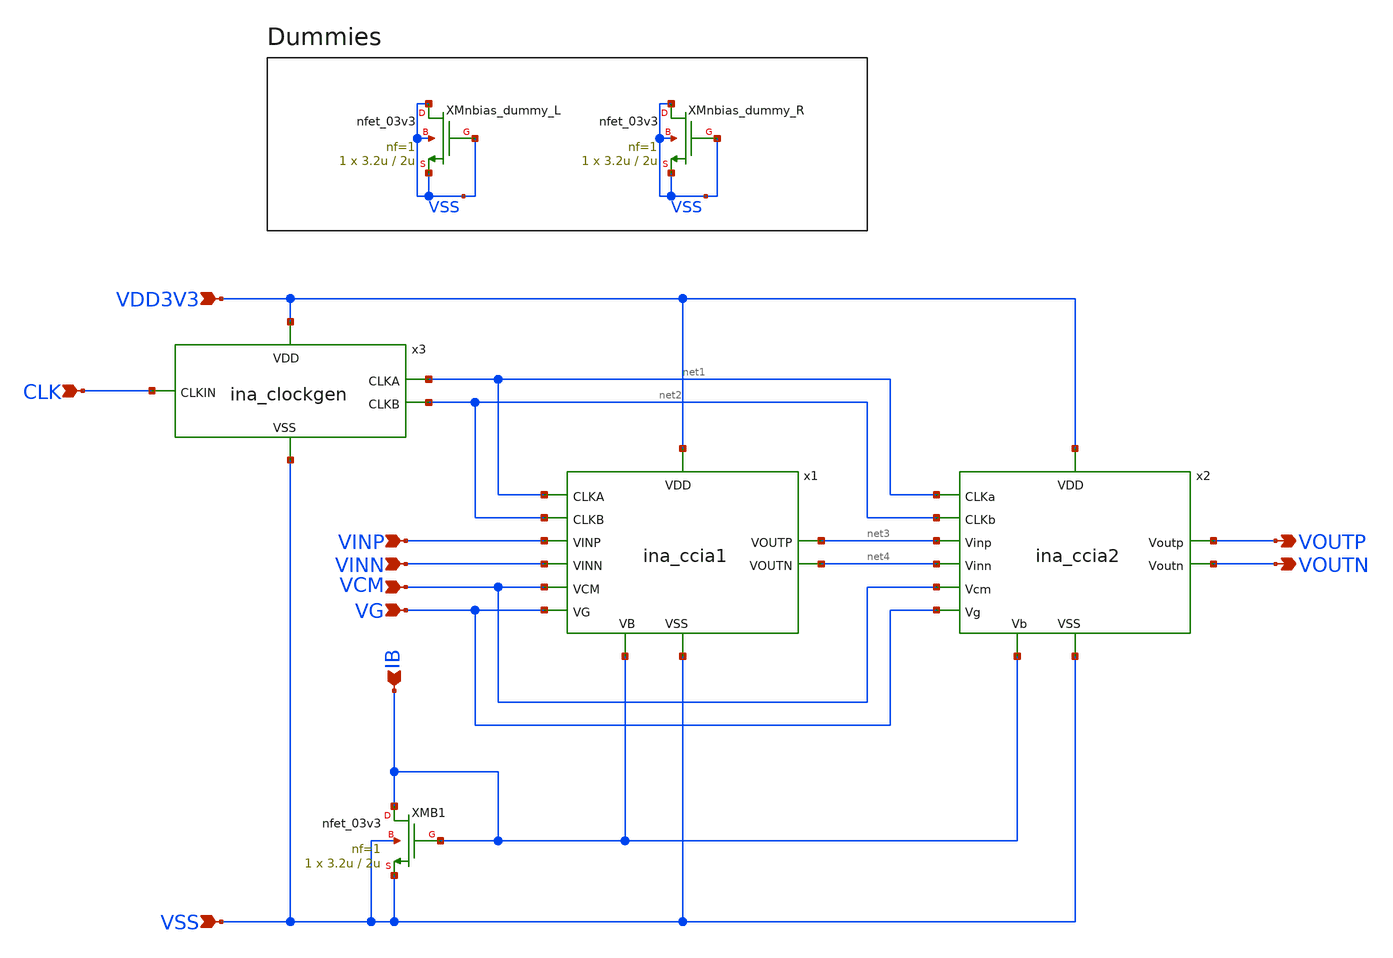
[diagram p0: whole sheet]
** sch_path: designs/libs/core_ina/ina/ina.sch
**.subckt ina CLK VINP VINN VDD3V3 VSS VCM IB VG VOUTP VOUTN
*.ipin CLK
*.ipin VINP
*.ipin VINN
*.ipin VDD3V3
*.ipin VSS
*.ipin VCM
*.ipin IB
*.ipin VG
*.opin VOUTP
*.opin VOUTN
x3 VDD3V3 CLK net1 net2 VSS ina_clockgen
XMB1 IB IB VSS VSS nfet_03v3 L=2u W=3.2u nf=1 ad='int((nf+1)/2) * W/nf * 0.18u' as='int((nf+2)/2) * W/nf * 0.18u'
+ pd='2*int((nf+1)/2) * (W/nf + 0.18u)' ps='2*int((nf+2)/2) * (W/nf + 0.18u)' nrd='0.18u / W' nrs='0.18u / W'
+ sa=0 sb=0 sd=0 m=1
XMnbias_dummy_L VSS VSS VSS VSS nfet_03v3 L=2u W=3.2u nf=1 ad='int((nf+1)/2) * W/nf * 0.18u' as='int((nf+2)/2) * W/nf * 0.18u'
+ pd='2*int((nf+1)/2) * (W/nf + 0.18u)' ps='2*int((nf+2)/2) * (W/nf + 0.18u)' nrd='0.18u / W' nrs='0.18u / W'
+ sa=0 sb=0 sd=0 m=1
XMnbias_dummy_R VSS VSS VSS VSS nfet_03v3 L=2u W=3.2u nf=1 ad='int((nf+1)/2) * W/nf * 0.18u' as='int((nf+2)/2) * W/nf * 0.18u'
+ pd='2*int((nf+1)/2) * (W/nf + 0.18u)' ps='2*int((nf+2)/2) * (W/nf + 0.18u)' nrd='0.18u / W' nrs='0.18u / W'
+ sa=0 sb=0 sd=0 m=1
x1 VG VINP VDD3V3 net3 VINN net4 net1 net2 VCM IB VSS ina_ccia1
x2 VG net3 VDD3V3 VOUTP net4 VOUTN net1 net2 VCM IB VSS ina_ccia2
**.ends
.end
